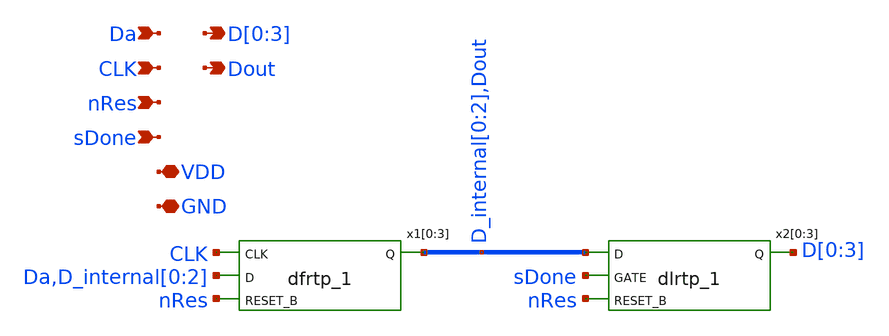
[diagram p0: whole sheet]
** sch_path: design/xschem/dflip_flop_chain_4_fc.sch
**.subckt dflip_flop_chain_4_fc Da D[0],D[1],D[2],D[3] CLK nRes sDone Dout VDD GND
*.ipin Da
*.opin D[0],D[1],D[2],D[3]
*.ipin CLK
*.ipin nRes
*.ipin sDone
*.opin Dout
*.iopin VDD
*.iopin GND
x1[0] CLK Da nRes GND GND VDD VDD D_internal[0] sky130_fd_sc_hd__dfrtp_1
x1[1] CLK D_internal[0] nRes GND GND VDD VDD D_internal[1] sky130_fd_sc_hd__dfrtp_1
x1[2] CLK D_internal[1] nRes GND GND VDD VDD D_internal[2] sky130_fd_sc_hd__dfrtp_1
x1[3] CLK D_internal[2] nRes GND GND VDD VDD Dout sky130_fd_sc_hd__dfrtp_1
x2[0] D_internal[0] sDone nRes GND GND VDD VDD D[0] sky130_fd_sc_hd__dlrtp_1
x2[1] D_internal[1] sDone nRes GND GND VDD VDD D[1] sky130_fd_sc_hd__dlrtp_1
x2[2] D_internal[2] sDone nRes GND GND VDD VDD D[2] sky130_fd_sc_hd__dlrtp_1
x2[3] Dout sDone nRes GND GND VDD VDD D[3] sky130_fd_sc_hd__dlrtp_1
**.ends
.end
